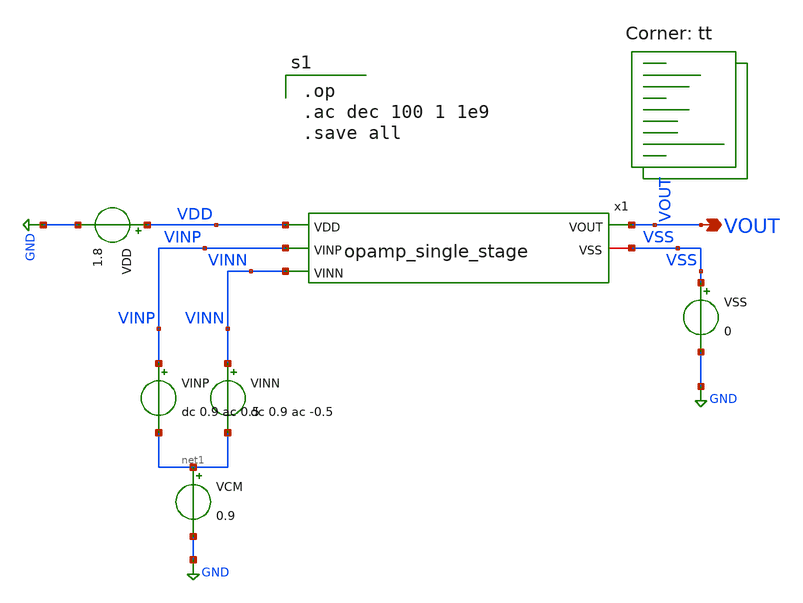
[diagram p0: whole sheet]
** sch_path: schematics/tb_ac_analysis.sch
**.subckt tb_ac_analysis VOUT
*.opin VOUT
VDD VDD GND 1.8
VCM net1 GND 0.9
VSS VSS GND 0
VINP VINP net1 dc 0.9 ac 0.5
VINN VINN net1 dc 0.9 ac -0.5
x1 VDD VOUT VINP VINN VSS opamp_single_stage
**** begin user architecture code

.op
.ac dec 100 1 1e9
.save all


.lib $::SKYWATER_MODELS/sky130.lib.spice tt
**** end user architecture code
**.ends
.GLOBAL GND
.end
